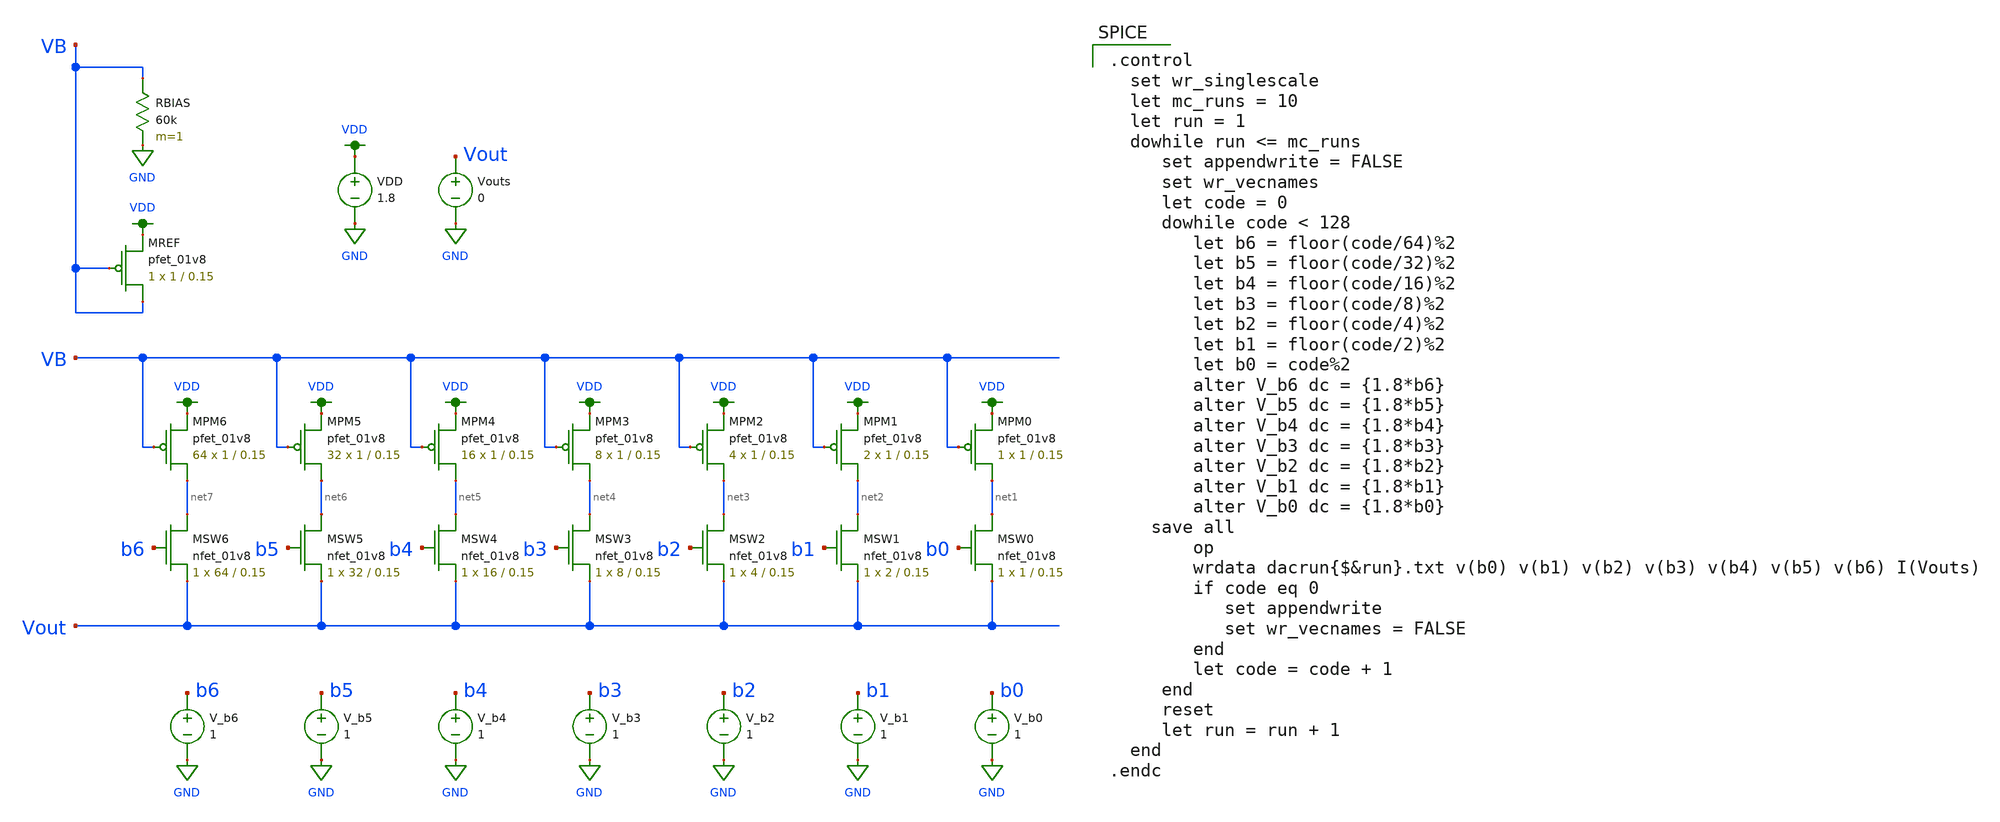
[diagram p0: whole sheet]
** sch_path: MP3/xschem/dac.sch
**.subckt dac
RBIAS VB GND 60k m=1
VDD VDD GND 1.8
XMREF VB VB VDD VDD sky130_fd_pr__pfet_01v8 L=0.15 W=1 nf=1 ad='int((nf+1)/2) * W/nf * 0.29' as='int((nf+2)/2) * W/nf * 0.29'
+ pd='2*int((nf+1)/2) * (W/nf + 0.29)' ps='2*int((nf+2)/2) * (W/nf + 0.29)' nrd='0.29 / W' nrs='0.29 / W'
+ sa=0 sb=0 sd=0 mult=1 m=1
XMPM6 net7 VB VDD VDD sky130_fd_pr__pfet_01v8 L=0.15 W=1 nf=1 ad='int((nf+1)/2) * W/nf * 0.29' as='int((nf+2)/2) * W/nf * 0.29'
+ pd='2*int((nf+1)/2) * (W/nf + 0.29)' ps='2*int((nf+2)/2) * (W/nf + 0.29)' nrd='0.29 / W' nrs='0.29 / W'
+ sa=0 sb=0 sd=0 mult=64 m=64
XMPM5 net6 VB VDD VDD sky130_fd_pr__pfet_01v8 L=0.15 W=1 nf=1 ad='int((nf+1)/2) * W/nf * 0.29' as='int((nf+2)/2) * W/nf * 0.29'
+ pd='2*int((nf+1)/2) * (W/nf + 0.29)' ps='2*int((nf+2)/2) * (W/nf + 0.29)' nrd='0.29 / W' nrs='0.29 / W'
+ sa=0 sb=0 sd=0 mult=32 m=32
XMPM4 net5 VB VDD VDD sky130_fd_pr__pfet_01v8 L=0.15 W=1 nf=1 ad='int((nf+1)/2) * W/nf * 0.29' as='int((nf+2)/2) * W/nf * 0.29'
+ pd='2*int((nf+1)/2) * (W/nf + 0.29)' ps='2*int((nf+2)/2) * (W/nf + 0.29)' nrd='0.29 / W' nrs='0.29 / W'
+ sa=0 sb=0 sd=0 mult=16 m=16
XMPM3 net4 VB VDD VDD sky130_fd_pr__pfet_01v8 L=0.15 W=1 nf=1 ad='int((nf+1)/2) * W/nf * 0.29' as='int((nf+2)/2) * W/nf * 0.29'
+ pd='2*int((nf+1)/2) * (W/nf + 0.29)' ps='2*int((nf+2)/2) * (W/nf + 0.29)' nrd='0.29 / W' nrs='0.29 / W'
+ sa=0 sb=0 sd=0 mult=8 m=8
XMPM2 net3 VB VDD VDD sky130_fd_pr__pfet_01v8 L=0.15 W=1 nf=1 ad='int((nf+1)/2) * W/nf * 0.29' as='int((nf+2)/2) * W/nf * 0.29'
+ pd='2*int((nf+1)/2) * (W/nf + 0.29)' ps='2*int((nf+2)/2) * (W/nf + 0.29)' nrd='0.29 / W' nrs='0.29 / W'
+ sa=0 sb=0 sd=0 mult=4 m=4
XMPM1 net2 VB VDD VDD sky130_fd_pr__pfet_01v8 L=0.15 W=1 nf=1 ad='int((nf+1)/2) * W/nf * 0.29' as='int((nf+2)/2) * W/nf * 0.29'
+ pd='2*int((nf+1)/2) * (W/nf + 0.29)' ps='2*int((nf+2)/2) * (W/nf + 0.29)' nrd='0.29 / W' nrs='0.29 / W'
+ sa=0 sb=0 sd=0 mult=2 m=2
XMPM0 net1 VB VDD VDD sky130_fd_pr__pfet_01v8 L=0.15 W=1 nf=1 ad='int((nf+1)/2) * W/nf * 0.29' as='int((nf+2)/2) * W/nf * 0.29'
+ pd='2*int((nf+1)/2) * (W/nf + 0.29)' ps='2*int((nf+2)/2) * (W/nf + 0.29)' nrd='0.29 / W' nrs='0.29 / W'
+ sa=0 sb=0 sd=0 mult=1 m=1
XMSW0 net1 b0 Vout GND sky130_fd_pr__nfet_01v8 L=0.15 W=1 nf=1 ad='int((nf+1)/2) * W/nf * 0.29' as='int((nf+2)/2) * W/nf * 0.29'
+ pd='2*int((nf+1)/2) * (W/nf + 0.29)' ps='2*int((nf+2)/2) * (W/nf + 0.29)' nrd='0.29 / W' nrs='0.29 / W'
+ sa=0 sb=0 sd=0 mult=1 m=1
XMSW1 net2 b1 Vout GND sky130_fd_pr__nfet_01v8 L=0.15 W=2 nf=1 ad='int((nf+1)/2) * W/nf * 0.29' as='int((nf+2)/2) * W/nf * 0.29'
+ pd='2*int((nf+1)/2) * (W/nf + 0.29)' ps='2*int((nf+2)/2) * (W/nf + 0.29)' nrd='0.29 / W' nrs='0.29 / W'
+ sa=0 sb=0 sd=0 mult=1 m=1
XMSW2 net3 b2 Vout GND sky130_fd_pr__nfet_01v8 L=0.15 W=4 nf=1 ad='int((nf+1)/2) * W/nf * 0.29' as='int((nf+2)/2) * W/nf * 0.29'
+ pd='2*int((nf+1)/2) * (W/nf + 0.29)' ps='2*int((nf+2)/2) * (W/nf + 0.29)' nrd='0.29 / W' nrs='0.29 / W'
+ sa=0 sb=0 sd=0 mult=1 m=1
XMSW3 net4 b3 Vout GND sky130_fd_pr__nfet_01v8 L=0.15 W=8 nf=1 ad='int((nf+1)/2) * W/nf * 0.29' as='int((nf+2)/2) * W/nf * 0.29'
+ pd='2*int((nf+1)/2) * (W/nf + 0.29)' ps='2*int((nf+2)/2) * (W/nf + 0.29)' nrd='0.29 / W' nrs='0.29 / W'
+ sa=0 sb=0 sd=0 mult=1 m=1
XMSW4 net5 b4 Vout GND sky130_fd_pr__nfet_01v8 L=0.15 W=16 nf=1 ad='int((nf+1)/2) * W/nf * 0.29' as='int((nf+2)/2) * W/nf * 0.29'
+ pd='2*int((nf+1)/2) * (W/nf + 0.29)' ps='2*int((nf+2)/2) * (W/nf + 0.29)' nrd='0.29 / W' nrs='0.29 / W'
+ sa=0 sb=0 sd=0 mult=1 m=1
XMSW5 net6 b5 Vout GND sky130_fd_pr__nfet_01v8 L=0.15 W=32 nf=1 ad='int((nf+1)/2) * W/nf * 0.29' as='int((nf+2)/2) * W/nf * 0.29'
+ pd='2*int((nf+1)/2) * (W/nf + 0.29)' ps='2*int((nf+2)/2) * (W/nf + 0.29)' nrd='0.29 / W' nrs='0.29 / W'
+ sa=0 sb=0 sd=0 mult=1 m=1
XMSW6 net7 b6 Vout GND sky130_fd_pr__nfet_01v8 L=0.15 W=64 nf=1 ad='int((nf+1)/2) * W/nf * 0.29' as='int((nf+2)/2) * W/nf * 0.29'
+ pd='2*int((nf+1)/2) * (W/nf + 0.29)' ps='2*int((nf+2)/2) * (W/nf + 0.29)' nrd='0.29 / W' nrs='0.29 / W'
+ sa=0 sb=0 sd=0 mult=1 m=1
V_b0 b0 GND 1
V_b1 b1 GND 1
V_b2 b2 GND 1
V_b3 b3 GND 1
V_b4 b4 GND 1
V_b5 b5 GND 1
V_b6 b6 GND 1
Vouts Vout GND 0
**** begin user architecture code

.lib $::SKYWATER_MODELS/sky130.lib.spice tt


.control
  set wr_singlescale
  let mc_runs = 10
  let run = 1
  dowhile run <= mc_runs
     set appendwrite = FALSE
     set wr_vecnames
     let code = 0
     dowhile code < 128
        let b6 = floor(code/64)%2
        let b5 = floor(code/32)%2
        let b4 = floor(code/16)%2
        let b3 = floor(code/8)%2
        let b2 = floor(code/4)%2
        let b1 = floor(code/2)%2
        let b0 = code%2
        alter V_b6 dc = {1.8*b6}
        alter V_b5 dc = {1.8*b5}
        alter V_b4 dc = {1.8*b4}
        alter V_b3 dc = {1.8*b3}
        alter V_b2 dc = {1.8*b2}
        alter V_b1 dc = {1.8*b1}
        alter V_b0 dc = {1.8*b0}
	save all
        op
        wrdata dacrun{$&run}.txt v(b0) v(b1) v(b2) v(b3) v(b4) v(b5) v(b6) I(Vouts)
        if code eq 0
           set appendwrite
           set wr_vecnames = FALSE
        end
        let code = code + 1
     end
     reset
     let run = run + 1
  end
.endc

**** end user architecture code
**.ends
.GLOBAL VDD
.GLOBAL GND
.end
